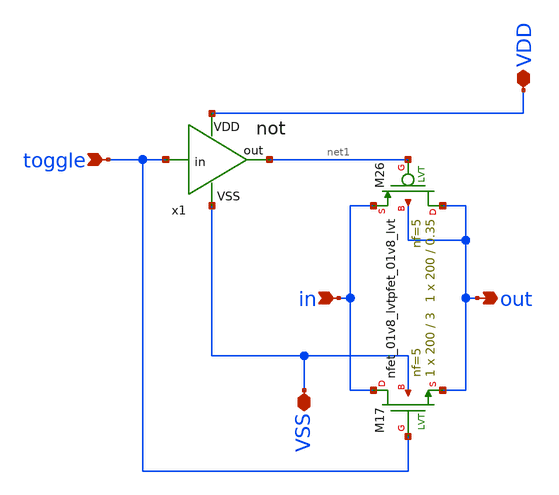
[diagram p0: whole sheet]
** sch_path: xschem/switch/switch.sch
**.subckt switch toggle in out VDD VSS
*.ipin toggle
*.ipin in
*.opin out
*.iopin VDD
*.iopin VSS
x1 VDD toggle net1 VSS not
XM26 out net1 in out sky130_fd_pr__pfet_01v8_lvt L=0.35 W=200 nf=5 ad='int((5 + 1)/2) * 200 / 5 * 0.29'
+ as='int((5 + 2)/2) * 200 / 5 * 0.29' pd='2*int((5 + 1)/2) * (200 / 5 + 0.29)' ps='2*int((5 + 2)/2) * (200 / 5 + 0.29)'
+ nrd='0.29 / 200 ' nrs='0.29 / 200 ' sa=0 sb=0 sd=0 mult=1 m=1
XM17 in toggle out VSS sky130_fd_pr__nfet_01v8_lvt L=3 W=200 nf=5 ad='int((5 + 1)/2) * 200 / 5 * 0.29'
+ as='int((5 + 2)/2) * 200 / 5 * 0.29' pd='2*int((5 + 1)/2) * (200 / 5 + 0.29)' ps='2*int((5 + 2)/2) * (200 / 5 + 0.29)'
+ nrd='0.29 / 200 ' nrs='0.29 / 200 ' sa=0 sb=0 sd=0 mult=1 m=1
**.ends

* expanding   symbol:  not/not.sym # of pins=4
** sym_path: xschem/not/not.sym
** sch_path: xschem/not/not.sch
.subckt not VDD in out VSS
*.ipin in
*.opin out
*.iopin VDD
*.iopin VSS
XM10 out in VDD VDD sky130_fd_pr__pfet_01v8_lvt L=0.35 W=2 nf=1 ad='int((1 + 1)/2) * 2 / 1 * 0.29' as='int((1 + 2)/2) * 2 / 1 * 0.29'
+ pd='2*int((1 + 1)/2) * (2 / 1 + 0.29)' ps='2*int((1 + 2)/2) * (2 / 1 + 0.29)' nrd='0.29 / 2 ' nrs='0.29 / 2 '
+ sa=0 sb=0 sd=0 mult=1 m=1
XM1 out in VSS VSS sky130_fd_pr__nfet_01v8_lvt L=0.35 W=1 nf=1 ad='int((1 + 1)/2) * 1 / 1 * 0.29' as='int((1 + 2)/2) * 1 / 1 * 0.29'
+ pd='2*int((1 + 1)/2) * (1 / 1 + 0.29)' ps='2*int((1 + 2)/2) * (1 / 1 + 0.29)' nrd='0.29 / 1 ' nrs='0.29 / 1 '
+ sa=0 sb=0 sd=0 mult=1 m=1
.ends

.end
